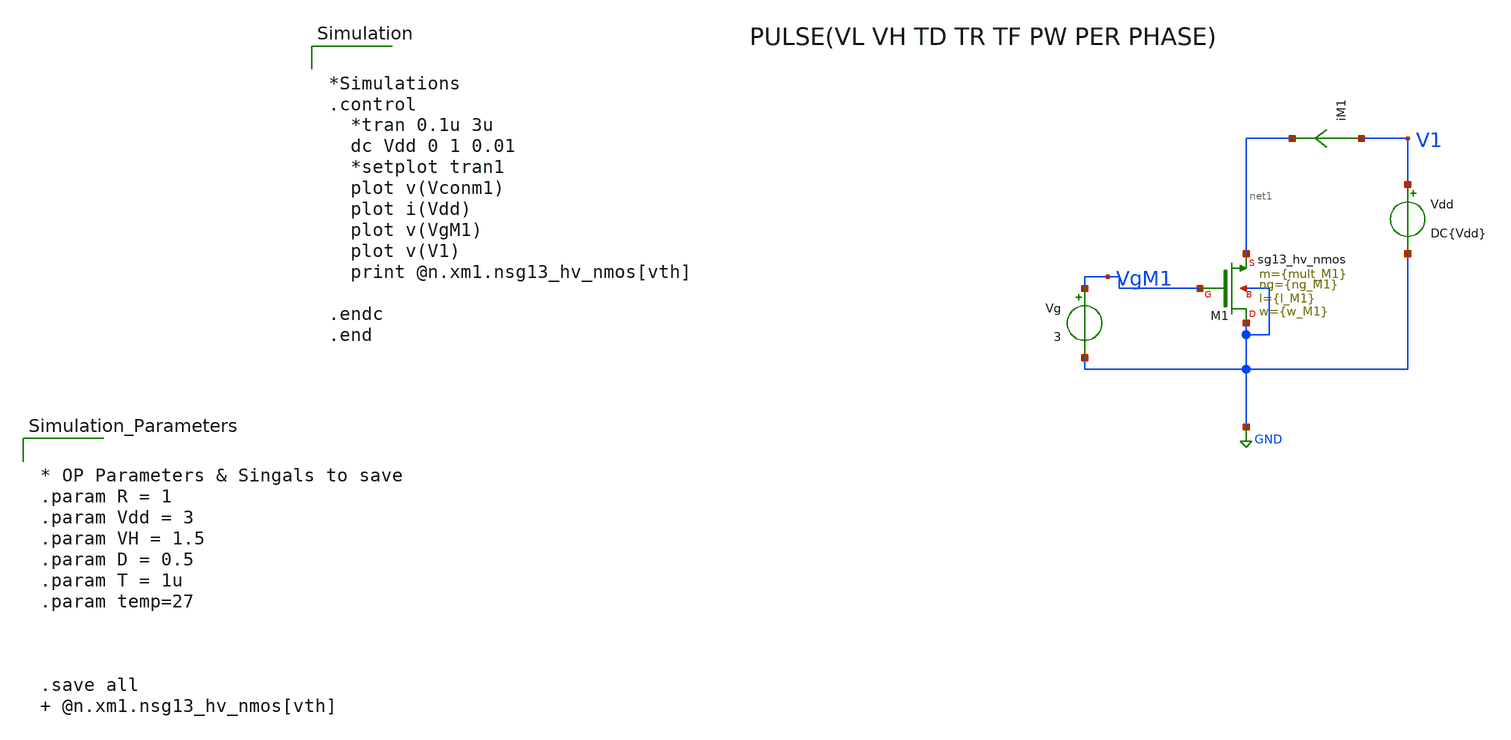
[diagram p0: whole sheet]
** sch_path: xschem/DCDCBuck/TB_hvNMOS_switch_test.sch
**.subckt TB_hvNMOS_switch_test
Vg VgM1 GND 3
Vdd V1 GND DC{Vdd}
iM1 V1 net1 0
.save i(im1)
XM1 GND VgM1 net1 GND sg13_hv_nmos w={w_M1} l={l_M1} ng={ng_M1} m={mult_M1} mm_ok=1
**** begin user architecture code


*Simulations
.control
  *tran 0.1u 3u
  dc Vdd 0 1 0.01
  *setplot tran1
  plot v(Vconm1)
  plot i(Vdd)
  plot v(VgM1)
  plot v(V1)
  print @n.xm1.nsg13_hv_nmos[vth]

.endc
.end





.lib cornerMOShv.lib mos_tt



.param temp=27
.param mult_M1 = 100
.param w_M1 =10u
.param l_M1 =0.25u
.param ng_M1 =1





* OP Parameters & Singals to save
.param R = 1
.param Vdd = 3
.param VH = 1.5
.param D = 0.5
.param T = 1u
.param temp=27



.save all  @n.xm1.nsg13_hv_nmos[vth]



**** end user architecture code
**.ends
.GLOBAL GND
.end
